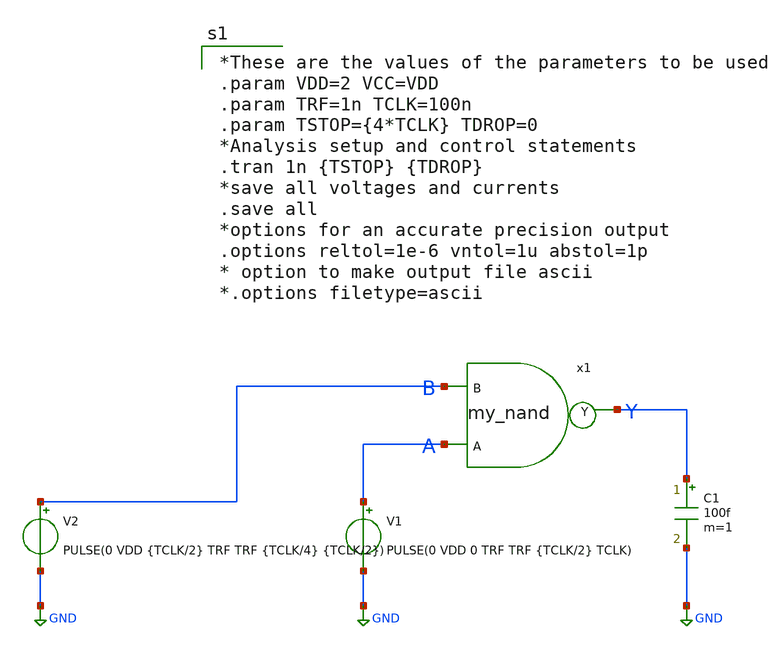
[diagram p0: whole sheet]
** sch_path: nand_test_bench.sch
**.subckt nand_test_bench
V1 A GND PULSE(0 VDD 0 TRF TRF {TCLK/2} TCLK)
C1 Y GND 100f m=1
V2 B GND PULSE(0 VDD {TCLK/2} TRF TRF {TCLK/4} {TCLK/2})
x1 B Y A my_nand
**** begin user architecture code

*These are the values of the parameters to be used
.param VDD=2 VCC=VDD
.param TRF=1n TCLK=100n
.param TSTOP={4*TCLK} TDROP=0
*Analysis setup and control statements
.tran 1n {TSTOP} {TDROP}
*save all voltages and currents
.save all
*options for an accurate precision output
.options reltol=1e-6 vntol=1u abstol=1p
* option to make output file ascii
*.options filetype=ascii


**** end user architecture code
**.ends

* expanding   symbol:  my_nand.sym # of pins=3
** sym_path: my_nand.sym
** sch_path: my_nand.sch
.subckt my_nand B Y A
*.ipin B
*.ipin A
*.opin Y
**** begin user architecture code

a6 [A B] Yi nand1
.model nand1 d_nand(rise_delay = 1e-9 fall_delay = 1e-9 input_load = 1e-12)

v1 Yi Y 0


**** end user architecture code
.ends

.GLOBAL GND
.end
